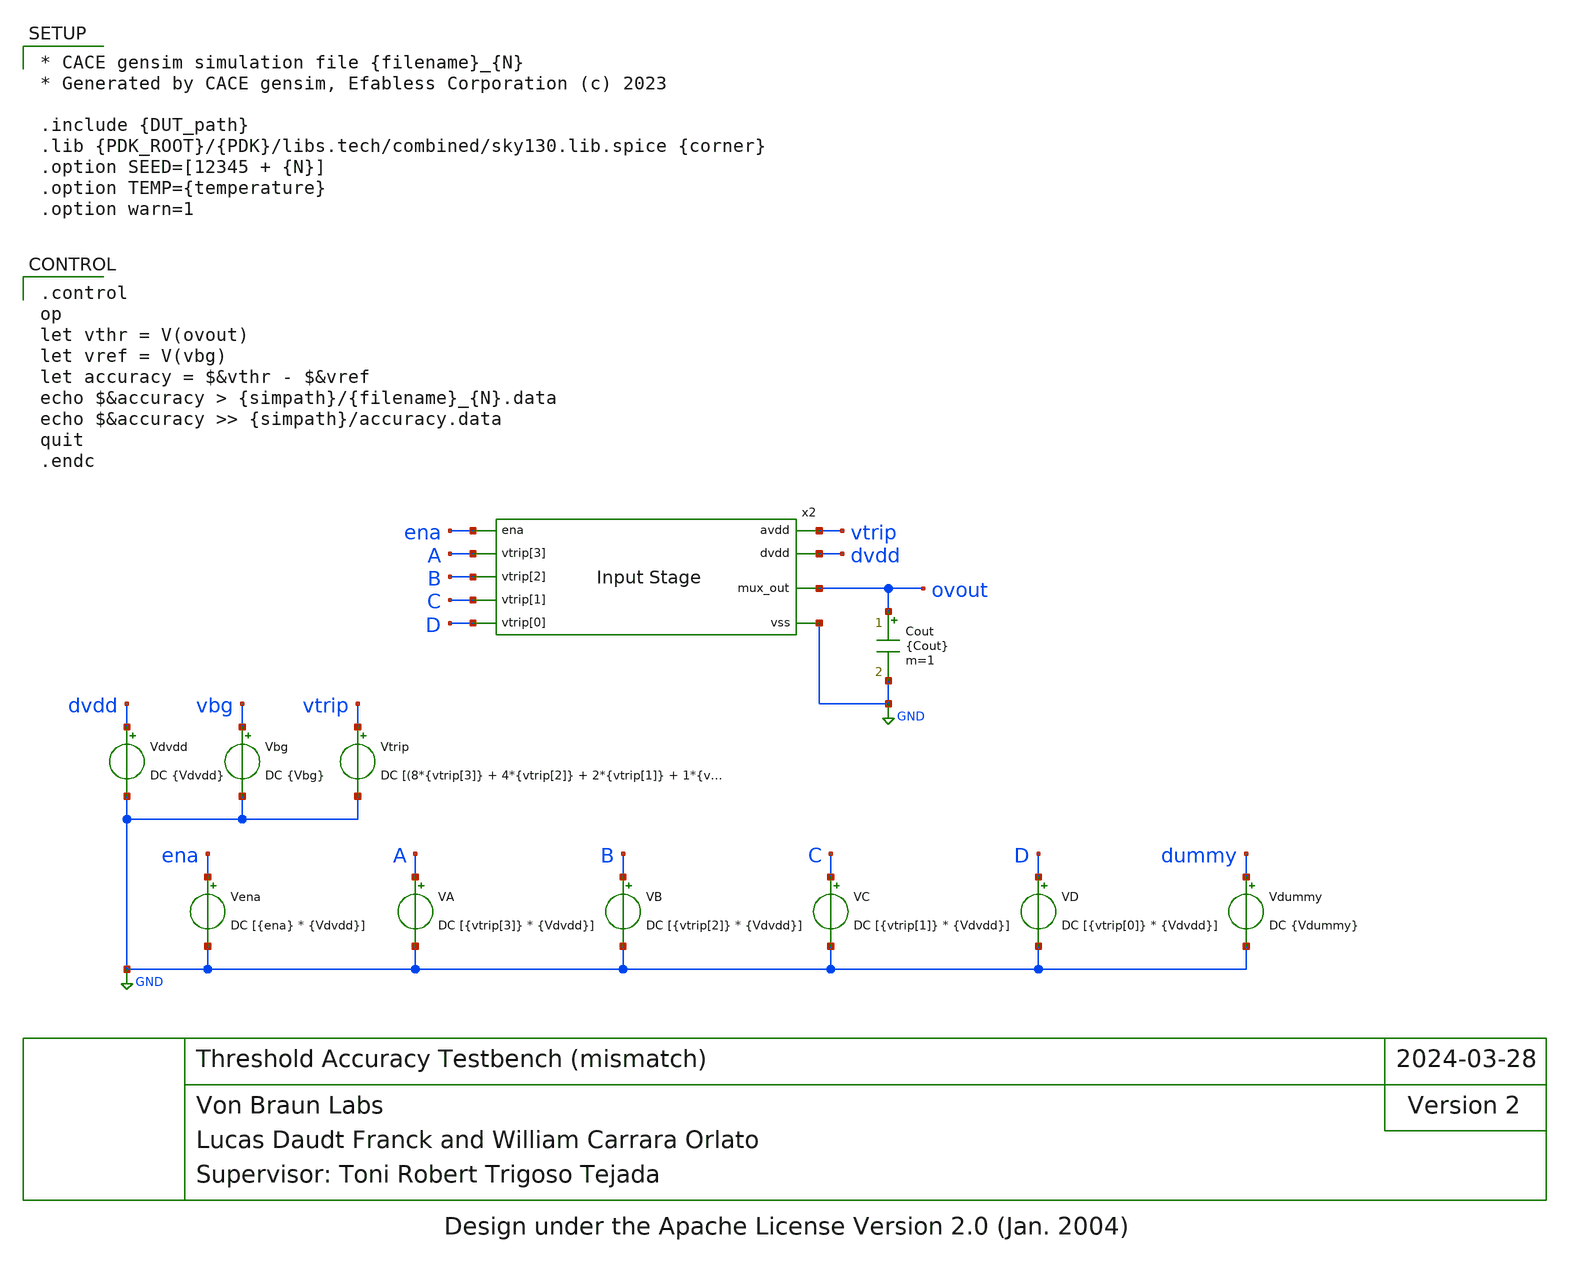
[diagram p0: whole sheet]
** sch_path: blocks/input/cace/tb_vacc_mm.sch
* Design under the Apache License Version 2.0 (Jan. 2004)
**.subckt tb_vacc_mm
Vena ena GND DC [{ena} * {Vdvdd}]
VA A GND DC [{vtrip[3]} * {Vdvdd}]
VB B GND DC [{vtrip[2]} * {Vdvdd}]
VC C GND DC [{vtrip[1]} * {Vdvdd}]
VD D GND DC [{vtrip[0]} * {Vdvdd}]
Vdummy dummy GND DC {Vdummy}
Vdvdd dvdd GND DC {Vdvdd}
Vbg vbg GND DC {Vbg}
Vtrip vtrip GND DC [(8*{vtrip[3]} + 4*{vtrip[2]} + 2*{vtrip[1]} + 1*{vtrip[0]})*0.14667 + 3.3]
x2 vtrip dvdd ena A GND B ovout C D input
Cout ovout GND {Cout} m=1
**** begin user architecture code

* CACE gensim simulation file {filename}_{N}
* Generated by CACE gensim, Efabless Corporation (c) 2023

.include {DUT_path}
.lib {PDK_ROOT}/{PDK}/libs.tech/combined/sky130.lib.spice {corner}
.option SEED=[12345 + {N}]
.option TEMP={temperature}
.option warn=1



.control
op
let vthr = V(ovout)
let vref = V(vbg)
let accuracy = $&vthr - $&vref
echo $&accuracy > {simpath}/{filename}_{N}.data
echo $&accuracy >> {simpath}/accuracy.data
quit
.endc


**** end user architecture code
**.ends
.GLOBAL GND
.end
